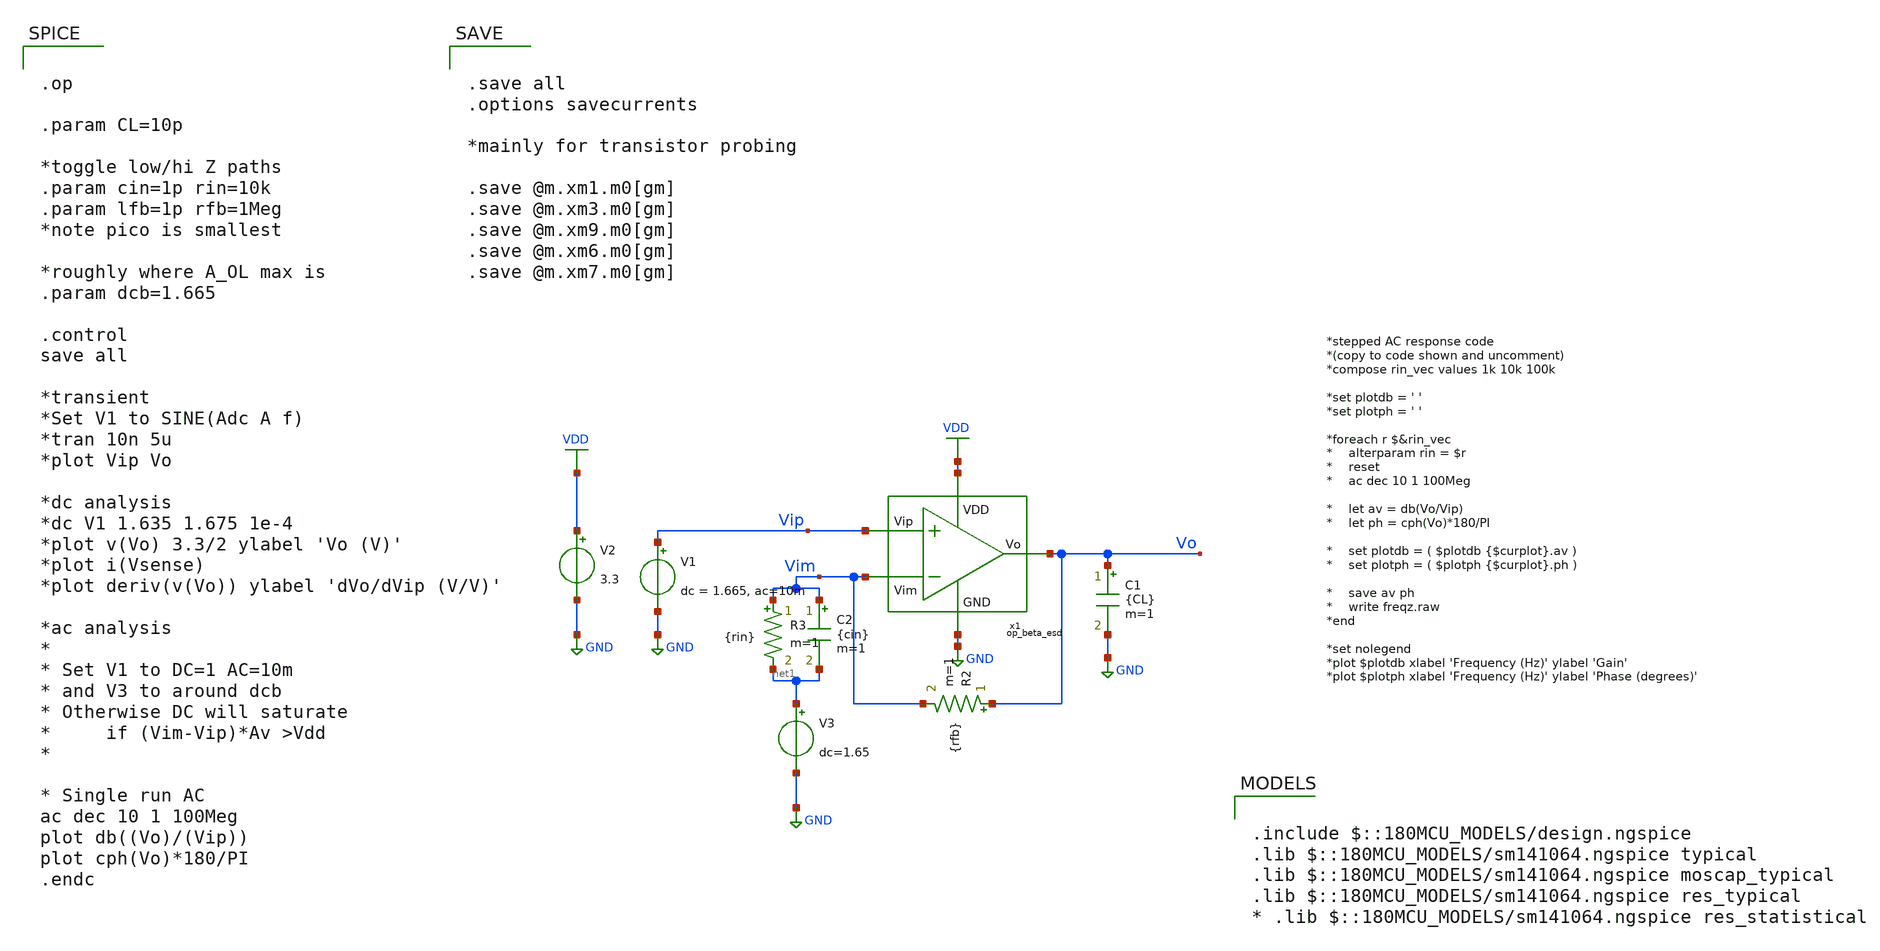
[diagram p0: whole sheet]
** sch_path: op_beta_esd_tb.sch
**.subckt op_beta_esd_tb
V1 Vip GND dc = 1.665, ac=10m
V2 VDD GND 3.3
C1 Vo GND {CL} m=1
R2 Vo Vim {rfb} m=1
R3 Vim net1 {rin} m=1
V3 net1 GND dc=1.65
C2 Vim net1 {cin} m=1
x1 VDD Vip Vo Vim GND op_beta_esd
**** begin user architecture code


.op

.param CL=10p

*toggle low/hi Z paths
.param cin=1p rin=10k
.param lfb=1p rfb=1Meg
*note pico is smallest

*roughly where A_OL max is
.param dcb=1.665

.control
save all

*transient
*Set V1 to SINE(Adc A f)
*tran 10n 5u
*plot Vip Vo

*dc analysis
*dc V1 1.635 1.675 1e-4
*plot v(Vo) 3.3/2 ylabel 'Vo (V)'
*plot i(Vsense)
*plot deriv(v(Vo)) ylabel 'dVo/dVip (V/V)'

*ac analysis
*
* Set V1 to DC=1 AC=10m
* and V3 to around dcb
* Otherwise DC will saturate
* 	if (Vim-Vip)*Av >Vdd
*

* Single run AC
ac dec 10 1 100Meg
plot db((Vo)/(Vip))
plot cph(Vo)*180/PI
.endc




.save all
.options savecurrents

*mainly for transistor probing

.save @m.xm1.m0[gm]
.save @m.xm3.m0[gm]
.save @m.xm9.m0[gm]
.save @m.xm6.m0[gm]
.save @m.xm7.m0[gm]




.include $::180MCU_MODELS/design.ngspice
.lib $::180MCU_MODELS/sm141064.ngspice typical
.lib $::180MCU_MODELS/sm141064.ngspice moscap_typical
.lib $::180MCU_MODELS/sm141064.ngspice res_typical
* .lib $::180MCU_MODELS/sm141064.ngspice res_statistical

**** end user architecture code
**.ends
.GLOBAL GND
.GLOBAL VDD
.end
